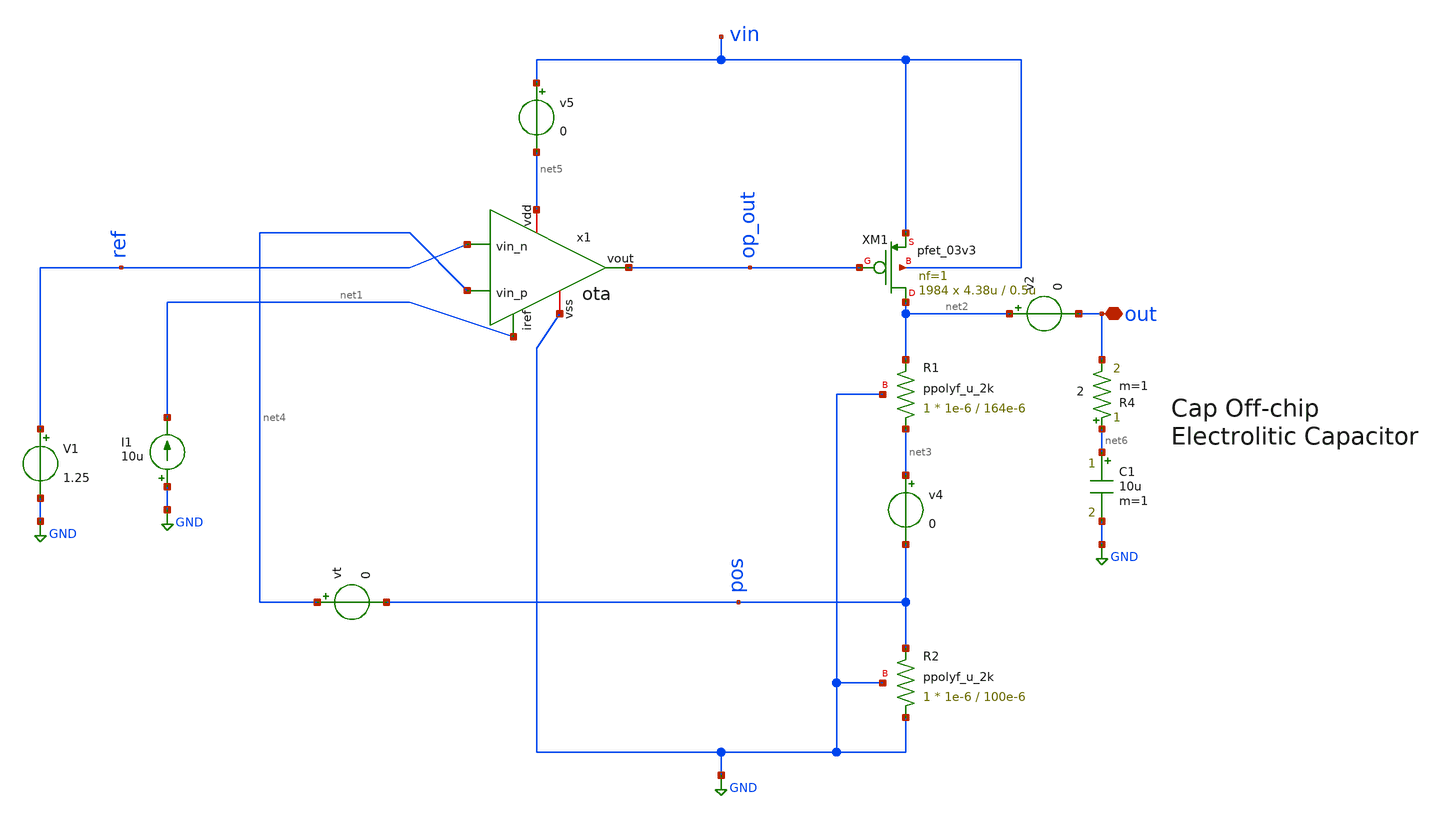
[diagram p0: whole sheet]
** sch_path: LDO/xschem/ldo/test/settling_time.sch

.include $env(PDK_ROOT)/$env(PDK)/libs.tech/ngspice/design.ngspice
.lib $env(PDK_ROOT)/$env(PDK)/libs.tech/ngspice/sm141064.ngspice typical
.lib $env(PDK_ROOT)/$env(PDK)/libs.tech/ngspice/sm141064.ngspice res_typical

.lib $env(PDK_ROOT)/$env(PDK)/libs.tech/ngspice/sm141064.ngspice cap_mim
.lib $env(PDK_ROOT)/$env(PDK)/libs.tech/ngspice/sm141064.ngspice mimcap_typical


**.subckt settling_time out
*.iopin out
I1 GND net1 10u
V1 ref GND 1.25
XM1 net2 op_out vin vin pfet_03v3 L=0.5u W=4.38u nf=1 ad='int((nf+1)/2) * W/nf * 0.18u' as='int((nf+2)/2) * W/nf * 0.18u'
+ pd='2*int((nf+1)/2) * (W/nf + 0.18u)' ps='2*int((nf+2)/2) * (W/nf + 0.18u)' nrd='0.18u / W' nrs='0.18u / W'
+ sa=0 sb=0 sd=0 m=1984
XR1 net3 net2 GND ppolyf_u_2k r_width=1e-6 r_length=164e-6 m=1
XR2 GND pos GND ppolyf_u_2k r_width=1e-6 r_length=100e-6 m=1
v4 net3 pos 0
vt net4 pos 0
v2 net2 out 0
v5 vin net5 0
x1 net5 net1 ref net4 op_out GND ota
C1 net6 GND 10u m=1
R4 net6 out 2 m=1
**** begin user architecture code


.param R=33
R10 out 0 {R}
IL out 0 PWL(0 0.1m 10u 0.1m 20u 10m 30u 10m)

.param iref = 10u
.param vdd  = 5
.param vss  = 0.0
.param vcm  = 1.25
.param vac  = 60m
.param w857 = 5u
.param l857 = 1u
.param m857 = 1
.param wpar = 10u
.param lpar = 1u
.param mpar = 1
.param w34  = 10u
.param l34  = 1u
.param m34  = 1
.param w6   = 100u
.param l6   = 1u
.param m6   = 1

.param m5   = 1
.param m7   = 5


Vs vin 0 5

.nodeset v(out)=0
.nodeset v(x1.pos)=0

*TRANSIENT
.control
save all
tran 1ns 200us
let gds = @x1.xm2.m0[gds]
print ic
plot gds
plot v(out) v(ref) v(pos) v(vin)
plot i(v5) i(v2)
plot v(op_out)
*plot v(op_out)
*plot v(out)
*plot i(out)
*plot i(v3)*v(vin)
.endc

*supply_sweep
.control
reseet
alter IL 0
dc Vs 6 0 -0.1
plot v(vin) v(out)
meas DC vldo_sup_4_6 FIND v(out) AT=4.6
meas DC vldo_nom FIND v(out) AT=5
meas DC vldo_sup_5_4 FIND v(out) AT=5.4
let line_reg = abs((vldo_sup_5_4-vldo_sup_4_6)/0.8)
print line_reg
meas DC vin WHEN v(out)=3.2982
let dropout = vin-3.2982
print dropout
.endc

*PSRR_Analysis
.control
reset
alter Vs AC =1
alter Vt AC=0
ac dec 100 1 1G
plot vdb(out)
let phase_val = 180/PI*cph(out)
plot phase_val
*plot (180/pi)*vp(out)
*let gm0=@m.xm0.m0[gm]
*let Zout=(1.5)/(gm0*v(op_out))
*let Zout2=v(out)/gm0
*plot vdb(Zout2)
*wrdata /foss/designs/LDO_Design/data/data_PSRR.dat vdb(out)
.endc

**Load_Transient
.control
reset
alter IL 50u
alter R10 3600k
tran 0.1u 100u
meas TRAN V_ldo_100u FIND v(out) AT=5u
meas TRAN V_ldo_10m FIND v(out) AT=100u
let load_reg= V_ldo_100u-V_ldo_10m
let load_current =(-1*i(Vs)-131.8e-6)
print load_reg/9.9
plot i(v2) v(out)-3.3
.endc

.control
alter R10 36k
reset
alter @IL[pwl]=[ 0 0 10u 0 20u 0 30u 0 ]
alter @Vs[pulse]=[ 5 4 50u 1u 1u 10u 100u ]
alter IL 0
tran 0.1u 100u
plot v(vin) v(out)
.endc


**** end user architecture code
**.ends
.GLOBAL GND
.end
